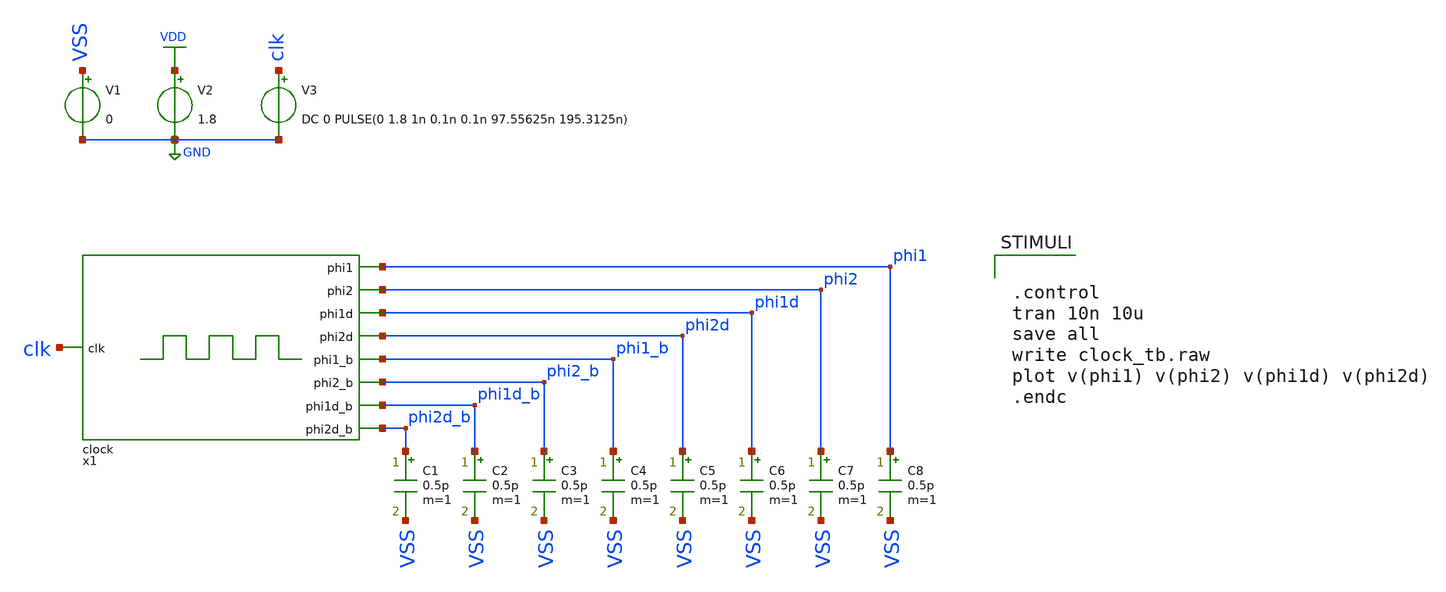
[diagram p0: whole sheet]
** sch_path: verification/schematic/clock_tb.sch
**.subckt clock_tb
x1 phi2 phi2_b phi2d clk phi2d_b phi1d_b phi1d phi1_b phi1 VDD VSS clock
V1 VSS GND 0
V2 VDD GND 1.8
V3 clk GND DC 0 PULSE(0 1.8 1n 0.1n 0.1n 97.55625n 195.3125n)
C1 phi2d_b VSS 0.5p m=1
C2 phi1d_b VSS 0.5p m=1
C3 phi2_b VSS 0.5p m=1
C4 phi1_b VSS 0.5p m=1
C5 phi2d VSS 0.5p m=1
C6 phi1d VSS 0.5p m=1
C7 phi2 VSS 0.5p m=1
C8 phi1 VSS 0.5p m=1
**** begin user architecture code

** opencircuitdesign pdks install
.lib /farmshare/home/classes/ee/372/PDKs/open_pdks_1.0.310/sky130/sky130A/libs.tech/ngspice/sky130.lib.spice tt
.inc /farmshare/home/classes/ee/372/PDKs/open_pdks_1.0.310/sky130/sky130A/libs.ref/sky130_fd_sc_hd/spice/sky130_fd_sc_hd.spice



.control
tran 10n 10u
save all
write clock_tb.raw
plot v(phi1) v(phi2) v(phi1d) v(phi2d)
.endc


**** end user architecture code
**.ends

* expanding   symbol:  clock.sym # of pins=9
** sym_path: design/schematic/clock.sym
** sch_path: design/schematic/clock.sch
.subckt clock phi2 phi2_b phi2d clk phi2d_b phi1d_b phi1d phi1_b phi1 VDD VSS
*.ipin clk
*.opin phi2d_b
*.opin phi2d
*.opin phi2_b
*.opin phi2
*.opin phi1d_b
*.opin phi1d
*.opin phi1_b
*.opin phi1
x2 clk net7 GND GND VDD VDD net1 sky130_fd_sc_hd__nand2_1
x3 net3 net6 GND GND VDD VDD net4 sky130_fd_sc_hd__nand2_1
x4 net1 GND GND VDD VDD phi2 sky130_fd_sc_hd__clkinv_1
x5 phi2 GND GND VDD VDD phi2_b sky130_fd_sc_hd__clkinv_1
x6 phi2_b GND GND VDD VDD net2 sky130_fd_sc_hd__clkinv_1
x8 phi2d GND GND VDD VDD phi2d_b sky130_fd_sc_hd__clkinv_4
x9 net4 GND GND VDD VDD phi1 sky130_fd_sc_hd__clkinv_1
x10 phi1 GND GND VDD VDD phi1_b sky130_fd_sc_hd__clkinv_1
x11 phi1_b GND GND VDD VDD net5 sky130_fd_sc_hd__clkinv_1
x13 phi1d GND GND VDD VDD phi1d_b sky130_fd_sc_hd__clkinv_4
x1 clk GND GND VDD VDD net3 sky130_fd_sc_hd__clkinv_1
x7 net2 GND GND VDD VDD phi2d sky130_fd_sc_hd__clkdlybuf4s50_1
x12 phi1d_b GND GND VDD VDD net7 sky130_fd_sc_hd__clkdlybuf4s50_1
x14 phi2d_b GND GND VDD VDD net6 sky130_fd_sc_hd__clkdlybuf4s50_1
x15 net5 GND GND VDD VDD phi1d sky130_fd_sc_hd__clkdlybuf4s50_1
.ends

.GLOBAL GND
.GLOBAL VDD
.end
